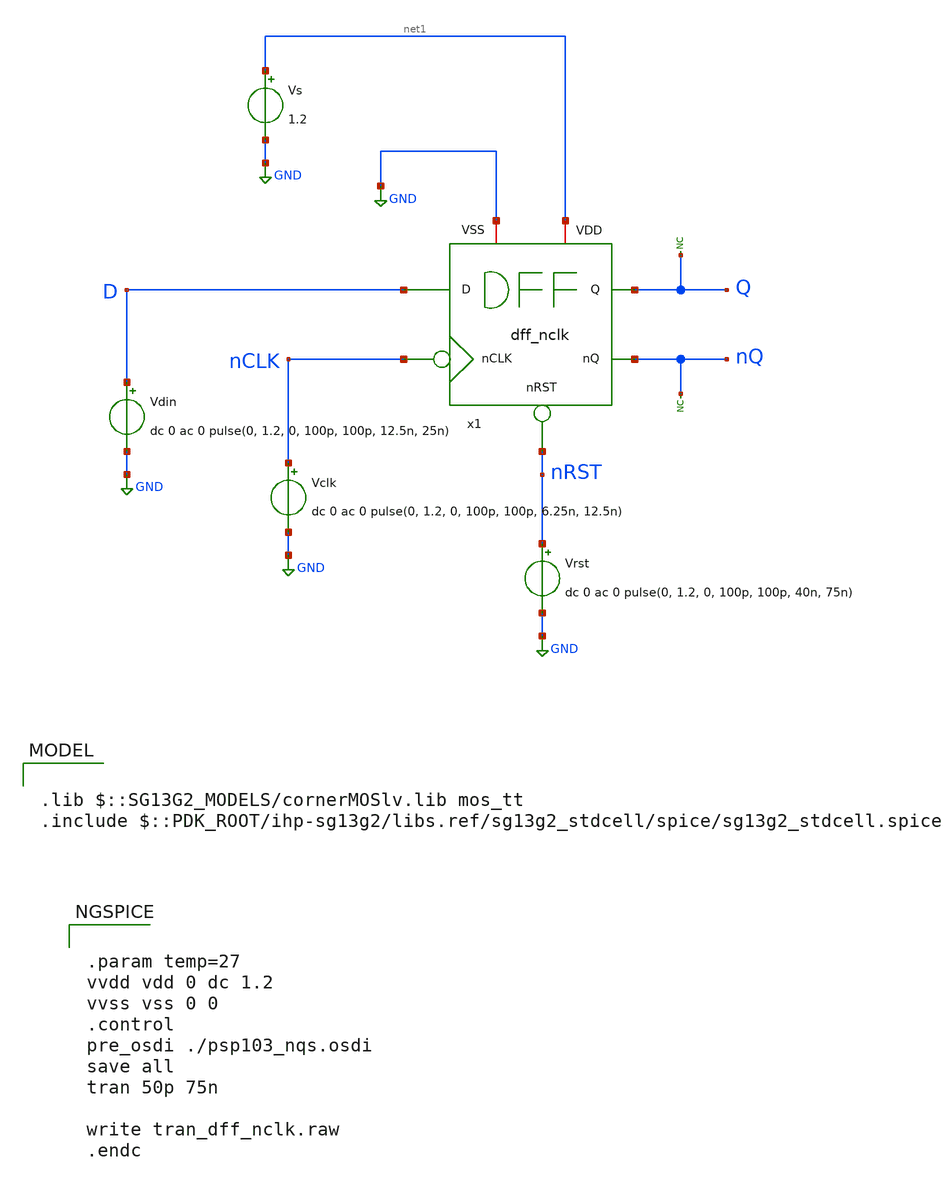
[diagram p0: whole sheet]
** sch_path: Combined Design/design_data/xschem/dff_nclk_tb.sch

.lib $::SG13G2_MODELS/cornerMOSlv.lib mos_tt
.include $::PDK_ROOT/ihp-sg13g2/libs.ref/sg13g2_stdcell/spice/sg13g2_stdcell.spice

**.subckt dff_nclk_tb
Vdin D GND dc 0 ac 0 pulse(0, 1.2, 0, 100p, 100p, 12.5n, 25n)
Vclk nCLK GND dc 0 ac 0 pulse(0, 1.2, 0, 100p, 100p, 6.25n, 12.5n)
Vrst nRST GND dc 0 ac 0 pulse(0, 1.2, 0, 100p, 100p, 40n, 75n)
* noconn nQ
* noconn Q
x1 nCLK Q D nQ nRST net1 GND dff_nclk
Vs net1 GND 1.2
**** begin user architecture code


.param temp=27
vvdd vdd 0 dc 1.2
vvss vss 0 0
.control
pre_osdi ./psp103_nqs.osdi
save all
tran 50p 75n

write tran_dff_nclk.raw
.endc


**** end user architecture code
**.ends
.GLOBAL GND
.end
